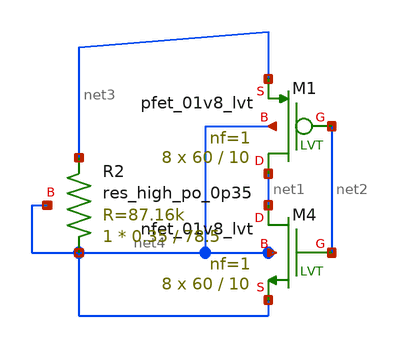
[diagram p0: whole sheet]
** sch_path: xschem/test.sch
**.subckt test
XM4 net1 net2 net4 net4 sky130_fd_pr__nfet_01v8_lvt L=10 W=60 nf=1 ad='int((nf+1)/2) * W/nf * 0.29' as='int((nf+2)/2) * W/nf * 0.29'
+ pd='2*int((nf+1)/2) * (W/nf + 0.29)' ps='2*int((nf+2)/2) * (W/nf + 0.29)' nrd='0.29 / W' nrs='0.29 / W'
+ sa=0 sb=0 sd=0 mult=8 m=8
XM1 net1 net2 net3 net4 sky130_fd_pr__pfet_01v8_lvt L=10 W=60 nf=1 ad='int((nf+1)/2) * W/nf * 0.29' as='int((nf+2)/2) * W/nf * 0.29'
+ pd='2*int((nf+1)/2) * (W/nf + 0.29)' ps='2*int((nf+2)/2) * (W/nf + 0.29)' nrd='0.29 / W' nrs='0.29 / W'
+ sa=0 sb=0 sd=0 mult=8 m=8
XR2 net4 net3 net4 sky130_fd_pr__res_high_po_0p35 L=78.5 mult=1 m=1
**.ends
.end
